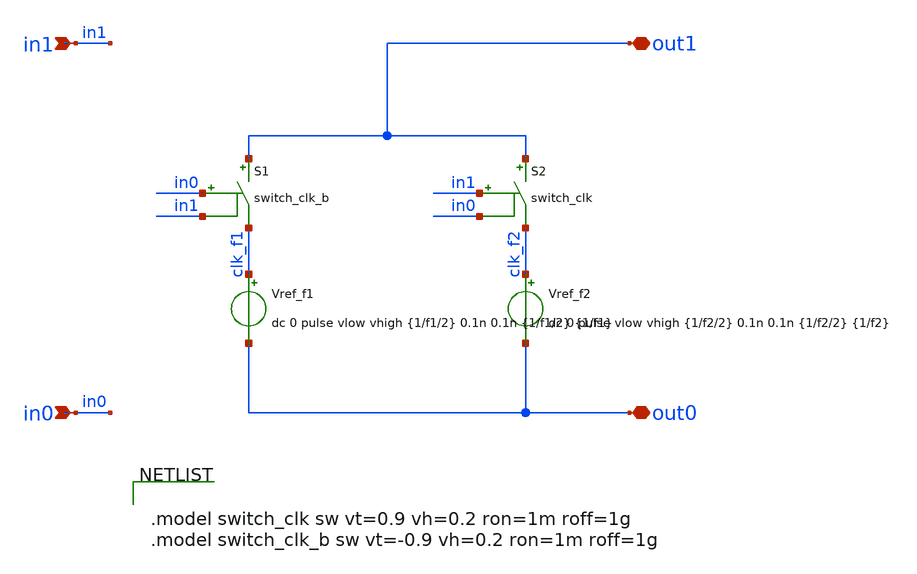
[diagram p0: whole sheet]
** sch_path: pll/pll_switch_freq_source/xschem/pll_switch_freq_source.sch
**.subckt pll_switch_freq_source out1 out0 in1 in0
*.iopin out1
*.iopin out0
*.ipin in1
*.ipin in0
Vref_f2 clk_f2 out0 dc 0 pulse vlow vhigh {1/f2/2} 0.1n 0.1n {1/f2/2} {1/f2}
Vref_f1 clk_f1 out0 dc 0 pulse vlow vhigh {1/f1/2} 0.1n 0.1n {1/f1/2} {1/f1}
S1 out1 clk_f1 in0 in1 switch_clk_b
S2 out1 clk_f2 in1 in0 switch_clk
**** begin user architecture code


.model switch_clk sw vt=0.9 vh=0.2 ron=1m roff=1g
.model switch_clk_b sw vt=-0.9 vh=0.2 ron=1m roff=1g


**** end user architecture code
**.ends
.end
